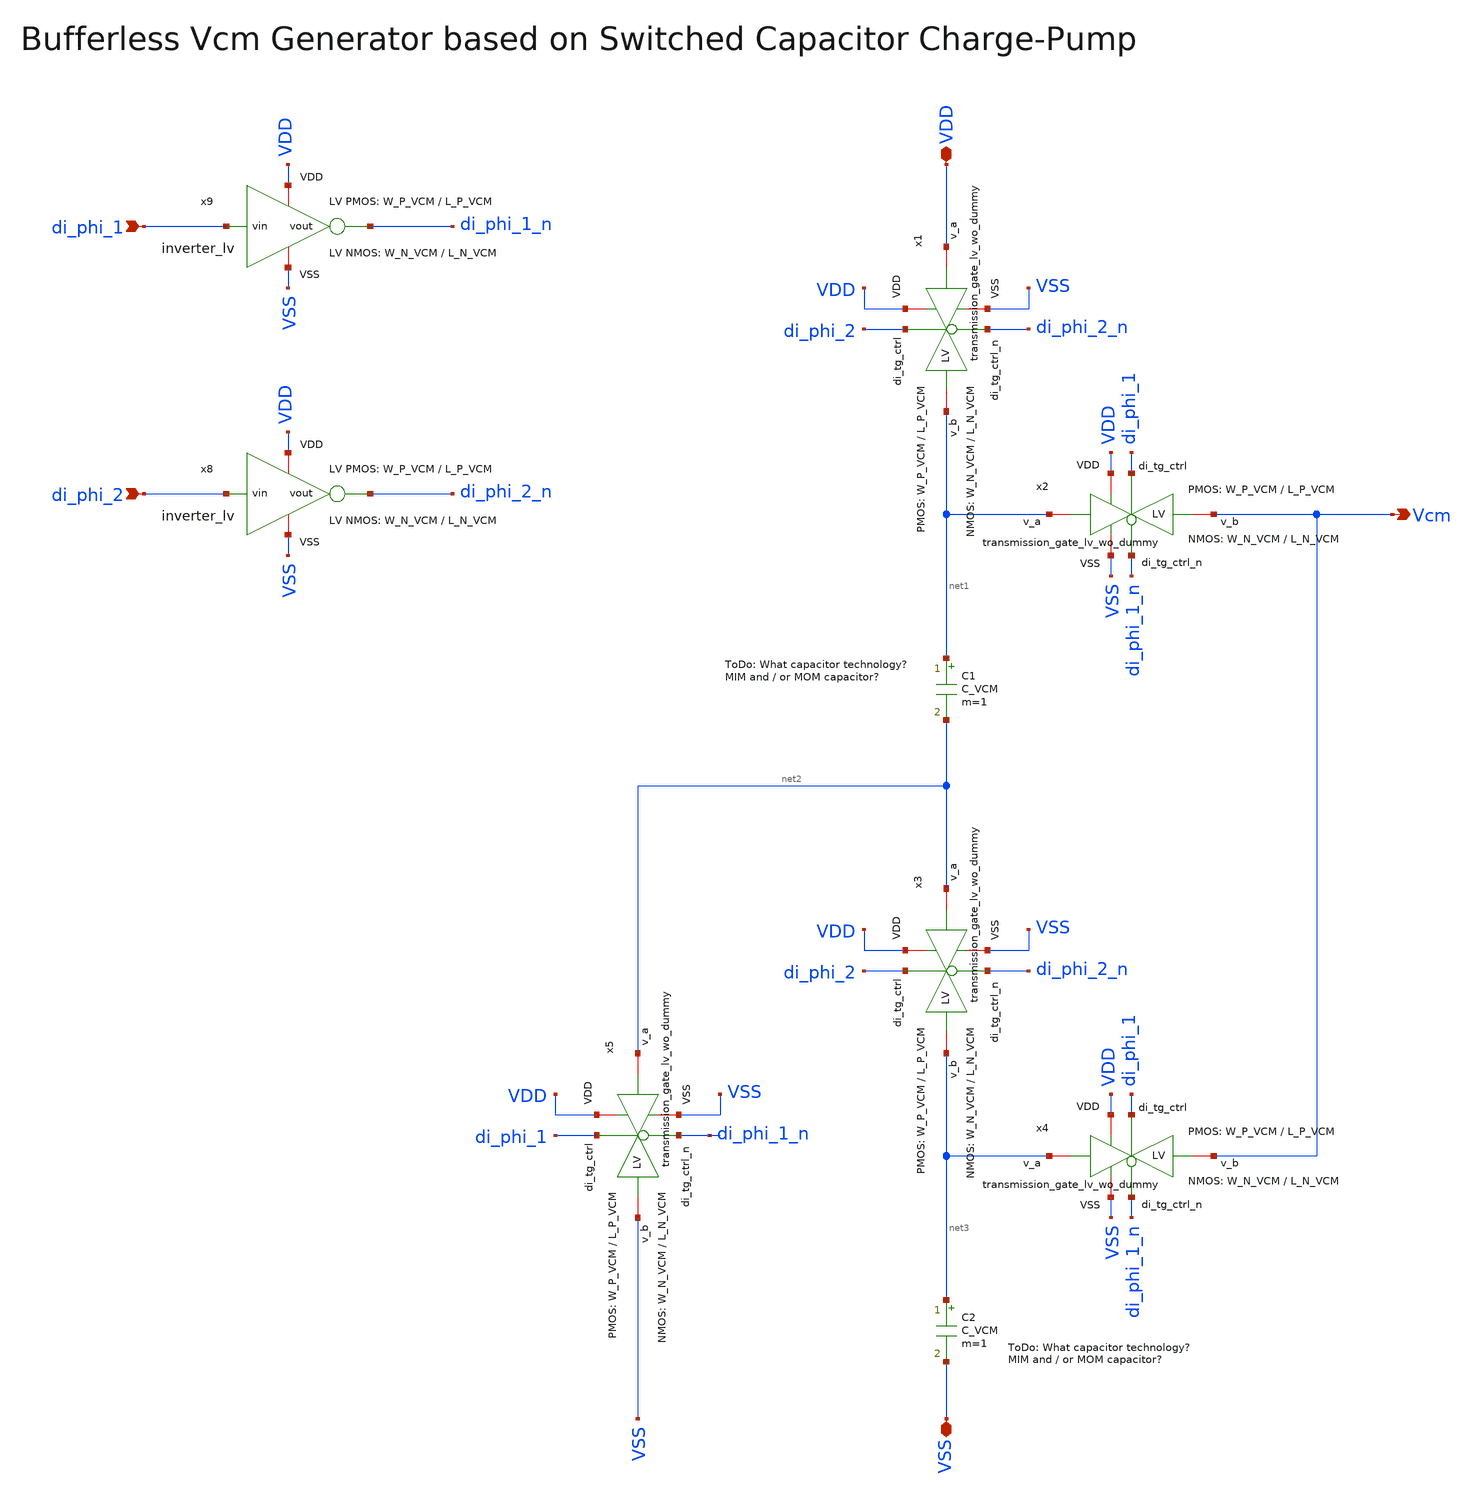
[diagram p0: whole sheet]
** sch_path: SG13G2_ATBS-ADC-main/xschem/vcm_generator/vcm_generator.sch
**.subckt vcm_generator VDD Vcm VSS di_phi_1 di_phi_2
*.iopin VDD
*.opin Vcm
*.iopin VSS
*.ipin di_phi_1
*.ipin di_phi_2
x1 VDD di_phi_2 VSS net1 VDD di_phi_2_n transmission_gate_lv_wo_dummy W_P=W_P_VCM L_P=L_P_VCM
+ W_N=W_N_VCM L_N=L_N_VCM
x2 VDD di_phi_1 VSS Vcm net1 di_phi_1_n transmission_gate_lv_wo_dummy W_P=W_P_VCM L_P=L_P_VCM
+ W_N=W_N_VCM L_N=L_N_VCM
x3 VDD di_phi_2 VSS net3 net2 di_phi_2_n transmission_gate_lv_wo_dummy W_P=W_P_VCM L_P=L_P_VCM
+ W_N=W_N_VCM L_N=L_N_VCM
x4 VDD di_phi_1 VSS Vcm net3 di_phi_1_n transmission_gate_lv_wo_dummy W_P=W_P_VCM L_P=L_P_VCM
+ W_N=W_N_VCM L_N=L_N_VCM
x5 VDD di_phi_1 VSS VSS net2 di_phi_1_n transmission_gate_lv_wo_dummy W_P=W_P_VCM L_P=L_P_VCM
+ W_N=W_N_VCM L_N=L_N_VCM
x9 VDD di_phi_1 di_phi_1_n VSS inverter_lv W_P=W_P_VCM L_P=L_P_VCM W_N=W_N_VCM L_N=L_N_VCM
x8 VDD di_phi_2 di_phi_2_n VSS inverter_lv W_P=W_P_VCM L_P=L_P_VCM W_N=W_N_VCM L_N=L_N_VCM
C1 net1 net2 C_VCM m=1
C2 net3 VSS C_VCM m=1
**.ends

* expanding   symbol:  transmission_gate/transmission_gate_lv_wo_dummy.sym # of pins=6
** sym_path: SG13G2_ATBS-ADC-main/xschem/transmission_gate/transmission_gate_lv_wo_dummy.sym
** sch_path: SG13G2_ATBS-ADC-main/xschem/transmission_gate/transmission_gate_lv_wo_dummy.sch
.subckt transmission_gate_lv_wo_dummy VDD di_tg_ctrl VSS v_b v_a di_tg_ctrl_n  W_P=1.0u L_P=0.13u
+ W_N=1.0u L_N=0.13u
*.iopin v_a
*.iopin v_b
*.iopin VDD
*.iopin VSS
*.ipin di_tg_ctrl
*.ipin di_tg_ctrl_n
XM1 v_a di_tg_ctrl v_b VSS sg13_lv_nmos w=W_N l=L_N ng=1 m=1 mm_ok=1
XM2 v_a di_tg_ctrl_n v_b VDD sg13_lv_pmos w=W_P l=L_P ng=1 m=1 mm_ok=1
.ends


* expanding   symbol:  inverter/inverter_lv.sym # of pins=4
** sym_path: SG13G2_ATBS-ADC-main/xschem/inverter/inverter_lv.sym
** sch_path: SG13G2_ATBS-ADC-main/xschem/inverter/inverter_lv.sch
.subckt inverter_lv VDD vin vout VSS  W_P=3.0u L_P=0.13u W_N=1.0u L_N=0.13u
*.ipin vin
*.iopin VDD
*.iopin VSS
*.opin vout
XM1 vout vin VDD VDD sg13_lv_pmos w=W_P l=L_P ng=1 m=1 mm_ok=1
XM2 vout vin VSS VSS sg13_lv_nmos w=W_N l=L_N ng=1 m=1 mm_ok=1
.ends

.end
